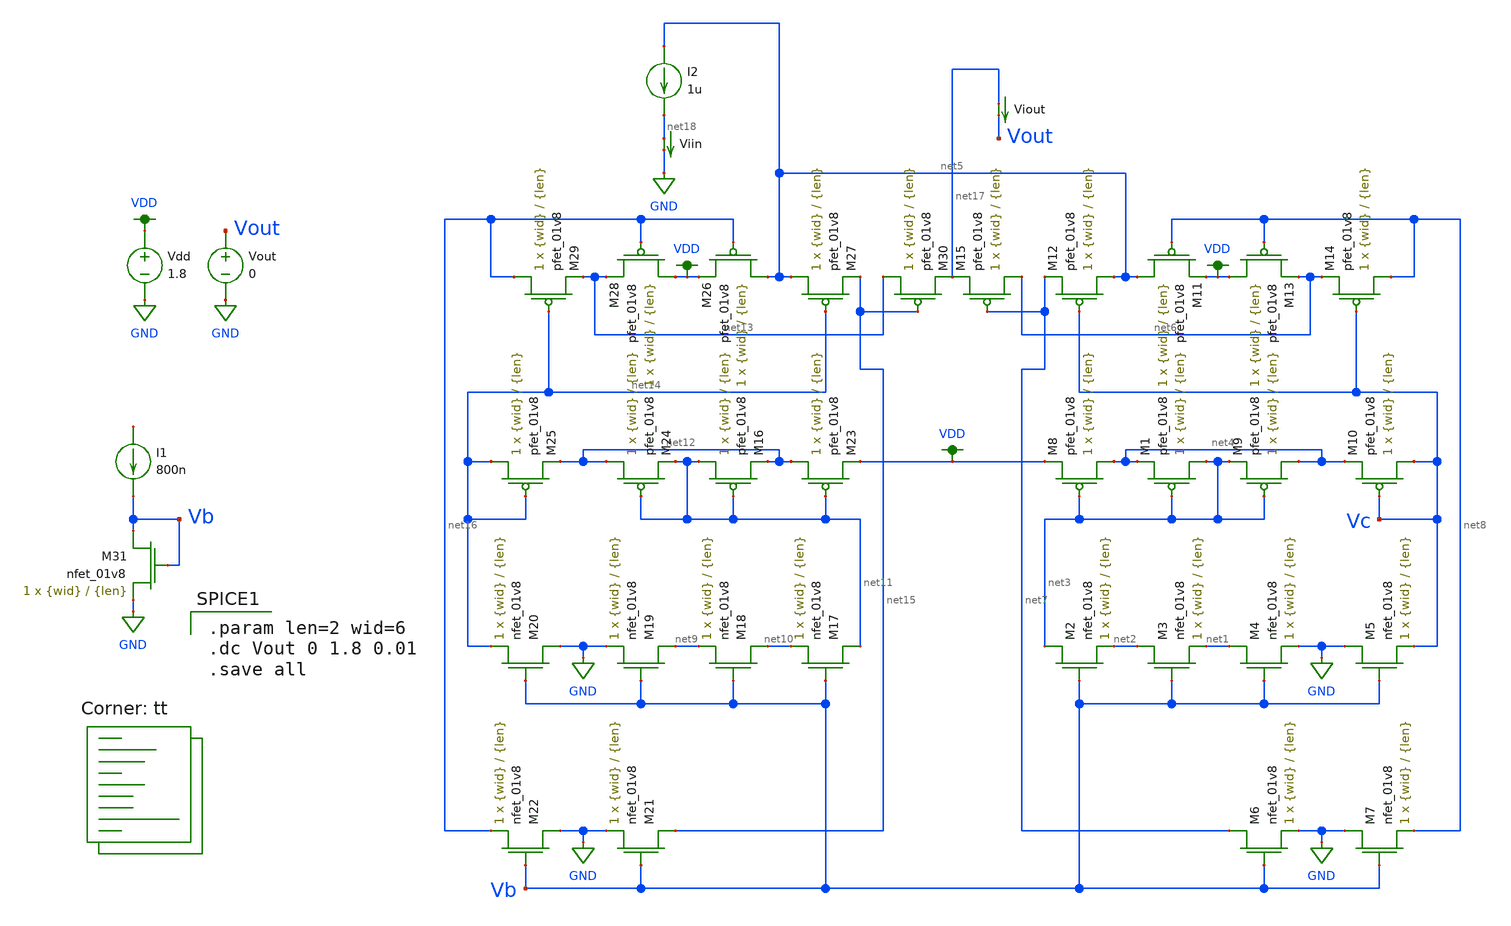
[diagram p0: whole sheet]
** sch_path: mp3/mirror_lvs_tb.sch
**.subckt mirror_lvs_tb
XM1 net3 net3 net4 VDD sky130_fd_pr__pfet_01v8 L={len} W={wid} nf=1 ad='int((nf+1)/2) * W/nf * 0.29'
+ as='int((nf+2)/2) * W/nf * 0.29' pd='2*int((nf+1)/2) * (W/nf + 0.29)' ps='2*int((nf+2)/2) * (W/nf + 0.29)'
+ nrd='0.29 / W' nrs='0.29 / W' sa=0 sb=0 sd=0 mult=1 m=1
XM2 net3 Vb net2 GND sky130_fd_pr__nfet_01v8 L={len} W={wid} nf=1 ad='int((nf+1)/2) * W/nf * 0.29' as='int((nf+2)/2) * W/nf * 0.29'
+ pd='2*int((nf+1)/2) * (W/nf + 0.29)' ps='2*int((nf+2)/2) * (W/nf + 0.29)' nrd='0.29 / W' nrs='0.29 / W'
+ sa=0 sb=0 sd=0 mult=1 m=1
XM3 net2 Vb net1 GND sky130_fd_pr__nfet_01v8 L={len} W={wid} nf=1 ad='int((nf+1)/2) * W/nf * 0.29' as='int((nf+2)/2) * W/nf * 0.29'
+ pd='2*int((nf+1)/2) * (W/nf + 0.29)' ps='2*int((nf+2)/2) * (W/nf + 0.29)' nrd='0.29 / W' nrs='0.29 / W'
+ sa=0 sb=0 sd=0 mult=1 m=1
XM4 net1 Vb GND GND sky130_fd_pr__nfet_01v8 L={len} W={wid} nf=1 ad='int((nf+1)/2) * W/nf * 0.29' as='int((nf+2)/2) * W/nf * 0.29'
+ pd='2*int((nf+1)/2) * (W/nf + 0.29)' ps='2*int((nf+2)/2) * (W/nf + 0.29)' nrd='0.29 / W' nrs='0.29 / W'
+ sa=0 sb=0 sd=0 mult=1 m=1
XM5 GND Vb Vc GND sky130_fd_pr__nfet_01v8 L={len} W={wid} nf=1 ad='int((nf+1)/2) * W/nf * 0.29' as='int((nf+2)/2) * W/nf * 0.29'
+ pd='2*int((nf+1)/2) * (W/nf + 0.29)' ps='2*int((nf+2)/2) * (W/nf + 0.29)' nrd='0.29 / W' nrs='0.29 / W'
+ sa=0 sb=0 sd=0 mult=1 m=1
XM6 net7 Vb GND GND sky130_fd_pr__nfet_01v8 L={len} W={wid} nf=1 ad='int((nf+1)/2) * W/nf * 0.29' as='int((nf+2)/2) * W/nf * 0.29'
+ pd='2*int((nf+1)/2) * (W/nf + 0.29)' ps='2*int((nf+2)/2) * (W/nf + 0.29)' nrd='0.29 / W' nrs='0.29 / W'
+ sa=0 sb=0 sd=0 mult=1 m=1
XM7 GND Vb net8 GND sky130_fd_pr__nfet_01v8 L={len} W={wid} nf=1 ad='int((nf+1)/2) * W/nf * 0.29' as='int((nf+2)/2) * W/nf * 0.29'
+ pd='2*int((nf+1)/2) * (W/nf + 0.29)' ps='2*int((nf+2)/2) * (W/nf + 0.29)' nrd='0.29 / W' nrs='0.29 / W'
+ sa=0 sb=0 sd=0 mult=1 m=1
XM8 net4 net3 VDD VDD sky130_fd_pr__pfet_01v8 L={len} W={wid} nf=1 ad='int((nf+1)/2) * W/nf * 0.29' as='int((nf+2)/2) * W/nf * 0.29'
+ pd='2*int((nf+1)/2) * (W/nf + 0.29)' ps='2*int((nf+2)/2) * (W/nf + 0.29)' nrd='0.29 / W' nrs='0.29 / W'
+ sa=0 sb=0 sd=0 mult=1 m=1
XM9 net4 net3 net3 VDD sky130_fd_pr__pfet_01v8 L={len} W={wid} nf=1 ad='int((nf+1)/2) * W/nf * 0.29'
+ as='int((nf+2)/2) * W/nf * 0.29' pd='2*int((nf+1)/2) * (W/nf + 0.29)' ps='2*int((nf+2)/2) * (W/nf + 0.29)'
+ nrd='0.29 / W' nrs='0.29 / W' sa=0 sb=0 sd=0 mult=1 m=1
XM10 Vc Vc net4 VDD sky130_fd_pr__pfet_01v8 L={len} W={wid} nf=1 ad='int((nf+1)/2) * W/nf * 0.29' as='int((nf+2)/2) * W/nf * 0.29'
+ pd='2*int((nf+1)/2) * (W/nf + 0.29)' ps='2*int((nf+2)/2) * (W/nf + 0.29)' nrd='0.29 / W' nrs='0.29 / W'
+ sa=0 sb=0 sd=0 mult=1 m=1
XM11 net5 net8 VDD VDD sky130_fd_pr__pfet_01v8 L={len} W={wid} nf=1 ad='int((nf+1)/2) * W/nf * 0.29'
+ as='int((nf+2)/2) * W/nf * 0.29' pd='2*int((nf+1)/2) * (W/nf + 0.29)' ps='2*int((nf+2)/2) * (W/nf + 0.29)'
+ nrd='0.29 / W' nrs='0.29 / W' sa=0 sb=0 sd=0 mult=1 m=1
XM12 net5 Vc net7 VDD sky130_fd_pr__pfet_01v8 L={len} W={wid} nf=1 ad='int((nf+1)/2) * W/nf * 0.29' as='int((nf+2)/2) * W/nf * 0.29'
+ pd='2*int((nf+1)/2) * (W/nf + 0.29)' ps='2*int((nf+2)/2) * (W/nf + 0.29)' nrd='0.29 / W' nrs='0.29 / W'
+ sa=0 sb=0 sd=0 mult=1 m=1
XM13 VDD net8 net6 VDD sky130_fd_pr__pfet_01v8 L={len} W={wid} nf=1 ad='int((nf+1)/2) * W/nf * 0.29'
+ as='int((nf+2)/2) * W/nf * 0.29' pd='2*int((nf+1)/2) * (W/nf + 0.29)' ps='2*int((nf+2)/2) * (W/nf + 0.29)'
+ nrd='0.29 / W' nrs='0.29 / W' sa=0 sb=0 sd=0 mult=1 m=1
XM14 net8 Vc net6 VDD sky130_fd_pr__pfet_01v8 L={len} W={wid} nf=1 ad='int((nf+1)/2) * W/nf * 0.29' as='int((nf+2)/2) * W/nf * 0.29'
+ pd='2*int((nf+1)/2) * (W/nf + 0.29)' ps='2*int((nf+2)/2) * (W/nf + 0.29)' nrd='0.29 / W' nrs='0.29 / W'
+ sa=0 sb=0 sd=0 mult=1 m=1
XM15 net6 net7 net17 VDD sky130_fd_pr__pfet_01v8 L={len} W={wid} nf=1 ad='int((nf+1)/2) * W/nf * 0.29'
+ as='int((nf+2)/2) * W/nf * 0.29' pd='2*int((nf+1)/2) * (W/nf + 0.29)' ps='2*int((nf+2)/2) * (W/nf + 0.29)'
+ nrd='0.29 / W' nrs='0.29 / W' sa=0 sb=0 sd=0 mult=1 m=1
XM16 net11 net11 net12 VDD sky130_fd_pr__pfet_01v8 L={len} W={wid} nf=1 ad='int((nf+1)/2) * W/nf * 0.29'
+ as='int((nf+2)/2) * W/nf * 0.29' pd='2*int((nf+1)/2) * (W/nf + 0.29)' ps='2*int((nf+2)/2) * (W/nf + 0.29)'
+ nrd='0.29 / W' nrs='0.29 / W' sa=0 sb=0 sd=0 mult=1 m=1
XM17 net11 Vb net10 GND sky130_fd_pr__nfet_01v8 L={len} W={wid} nf=1 ad='int((nf+1)/2) * W/nf * 0.29'
+ as='int((nf+2)/2) * W/nf * 0.29' pd='2*int((nf+1)/2) * (W/nf + 0.29)' ps='2*int((nf+2)/2) * (W/nf + 0.29)'
+ nrd='0.29 / W' nrs='0.29 / W' sa=0 sb=0 sd=0 mult=1 m=1
XM18 net10 Vb net9 GND sky130_fd_pr__nfet_01v8 L={len} W={wid} nf=1 ad='int((nf+1)/2) * W/nf * 0.29'
+ as='int((nf+2)/2) * W/nf * 0.29' pd='2*int((nf+1)/2) * (W/nf + 0.29)' ps='2*int((nf+2)/2) * (W/nf + 0.29)'
+ nrd='0.29 / W' nrs='0.29 / W' sa=0 sb=0 sd=0 mult=1 m=1
XM19 net9 Vb GND GND sky130_fd_pr__nfet_01v8 L={len} W={wid} nf=1 ad='int((nf+1)/2) * W/nf * 0.29' as='int((nf+2)/2) * W/nf * 0.29'
+ pd='2*int((nf+1)/2) * (W/nf + 0.29)' ps='2*int((nf+2)/2) * (W/nf + 0.29)' nrd='0.29 / W' nrs='0.29 / W'
+ sa=0 sb=0 sd=0 mult=1 m=1
XM20 GND Vb net14 GND sky130_fd_pr__nfet_01v8 L={len} W={wid} nf=1 ad='int((nf+1)/2) * W/nf * 0.29' as='int((nf+2)/2) * W/nf * 0.29'
+ pd='2*int((nf+1)/2) * (W/nf + 0.29)' ps='2*int((nf+2)/2) * (W/nf + 0.29)' nrd='0.29 / W' nrs='0.29 / W'
+ sa=0 sb=0 sd=0 mult=1 m=1
XM21 net15 Vb GND GND sky130_fd_pr__nfet_01v8 L={len} W={wid} nf=1 ad='int((nf+1)/2) * W/nf * 0.29' as='int((nf+2)/2) * W/nf * 0.29'
+ pd='2*int((nf+1)/2) * (W/nf + 0.29)' ps='2*int((nf+2)/2) * (W/nf + 0.29)' nrd='0.29 / W' nrs='0.29 / W'
+ sa=0 sb=0 sd=0 mult=1 m=1
XM22 GND Vb net16 GND sky130_fd_pr__nfet_01v8 L={len} W={wid} nf=1 ad='int((nf+1)/2) * W/nf * 0.29' as='int((nf+2)/2) * W/nf * 0.29'
+ pd='2*int((nf+1)/2) * (W/nf + 0.29)' ps='2*int((nf+2)/2) * (W/nf + 0.29)' nrd='0.29 / W' nrs='0.29 / W'
+ sa=0 sb=0 sd=0 mult=1 m=1
XM23 net12 net11 VDD VDD sky130_fd_pr__pfet_01v8 L={len} W={wid} nf=1 ad='int((nf+1)/2) * W/nf * 0.29'
+ as='int((nf+2)/2) * W/nf * 0.29' pd='2*int((nf+1)/2) * (W/nf + 0.29)' ps='2*int((nf+2)/2) * (W/nf + 0.29)'
+ nrd='0.29 / W' nrs='0.29 / W' sa=0 sb=0 sd=0 mult=1 m=1
XM24 net12 net11 net11 VDD sky130_fd_pr__pfet_01v8 L={len} W={wid} nf=1 ad='int((nf+1)/2) * W/nf * 0.29'
+ as='int((nf+2)/2) * W/nf * 0.29' pd='2*int((nf+1)/2) * (W/nf + 0.29)' ps='2*int((nf+2)/2) * (W/nf + 0.29)'
+ nrd='0.29 / W' nrs='0.29 / W' sa=0 sb=0 sd=0 mult=1 m=1
XM25 net14 net14 net12 VDD sky130_fd_pr__pfet_01v8 L={len} W={wid} nf=1 ad='int((nf+1)/2) * W/nf * 0.29'
+ as='int((nf+2)/2) * W/nf * 0.29' pd='2*int((nf+1)/2) * (W/nf + 0.29)' ps='2*int((nf+2)/2) * (W/nf + 0.29)'
+ nrd='0.29 / W' nrs='0.29 / W' sa=0 sb=0 sd=0 mult=1 m=1
XM26 net5 net16 VDD VDD sky130_fd_pr__pfet_01v8 L={len} W={wid} nf=1 ad='int((nf+1)/2) * W/nf * 0.29'
+ as='int((nf+2)/2) * W/nf * 0.29' pd='2*int((nf+1)/2) * (W/nf + 0.29)' ps='2*int((nf+2)/2) * (W/nf + 0.29)'
+ nrd='0.29 / W' nrs='0.29 / W' sa=0 sb=0 sd=0 mult=1 m=1
XM27 net5 net14 net15 VDD sky130_fd_pr__pfet_01v8 L={len} W={wid} nf=1 ad='int((nf+1)/2) * W/nf * 0.29'
+ as='int((nf+2)/2) * W/nf * 0.29' pd='2*int((nf+1)/2) * (W/nf + 0.29)' ps='2*int((nf+2)/2) * (W/nf + 0.29)'
+ nrd='0.29 / W' nrs='0.29 / W' sa=0 sb=0 sd=0 mult=1 m=1
XM28 VDD net16 net13 VDD sky130_fd_pr__pfet_01v8 L={len} W={wid} nf=1 ad='int((nf+1)/2) * W/nf * 0.29'
+ as='int((nf+2)/2) * W/nf * 0.29' pd='2*int((nf+1)/2) * (W/nf + 0.29)' ps='2*int((nf+2)/2) * (W/nf + 0.29)'
+ nrd='0.29 / W' nrs='0.29 / W' sa=0 sb=0 sd=0 mult=1 m=1
XM29 net16 net14 net13 VDD sky130_fd_pr__pfet_01v8 L={len} W={wid} nf=1 ad='int((nf+1)/2) * W/nf * 0.29'
+ as='int((nf+2)/2) * W/nf * 0.29' pd='2*int((nf+1)/2) * (W/nf + 0.29)' ps='2*int((nf+2)/2) * (W/nf + 0.29)'
+ nrd='0.29 / W' nrs='0.29 / W' sa=0 sb=0 sd=0 mult=1 m=1
XM30 net13 net15 net17 VDD sky130_fd_pr__pfet_01v8 L={len} W={wid} nf=1 ad='int((nf+1)/2) * W/nf * 0.29'
+ as='int((nf+2)/2) * W/nf * 0.29' pd='2*int((nf+1)/2) * (W/nf + 0.29)' ps='2*int((nf+2)/2) * (W/nf + 0.29)'
+ nrd='0.29 / W' nrs='0.29 / W' sa=0 sb=0 sd=0 mult=1 m=1
Vdd VDD GND 1.8
I1 net19 Vb 800n
XM31 Vb Vb GND GND sky130_fd_pr__nfet_01v8 L={len} W={wid} nf=1 ad='int((nf+1)/2) * W/nf * 0.29' as='int((nf+2)/2) * W/nf * 0.29'
+ pd='2*int((nf+1)/2) * (W/nf + 0.29)' ps='2*int((nf+2)/2) * (W/nf + 0.29)' nrd='0.29 / W' nrs='0.29 / W'
+ sa=0 sb=0 sd=0 mult=1 m=1
I2 net5 net18 1u
Vout Vout GND 0
Viout net17 Vout 0
.save i(viout)
Viin net18 GND 0
.save i(viin)
**** begin user architecture code
.lib $::SKYWATER_MODELS/sky130.lib.spice tt

.param len=2 wid=6
.dc Vout 0 1.8 0.01
.save all


**** end user architecture code
**.ends
.GLOBAL GND
.GLOBAL VDD
.end
